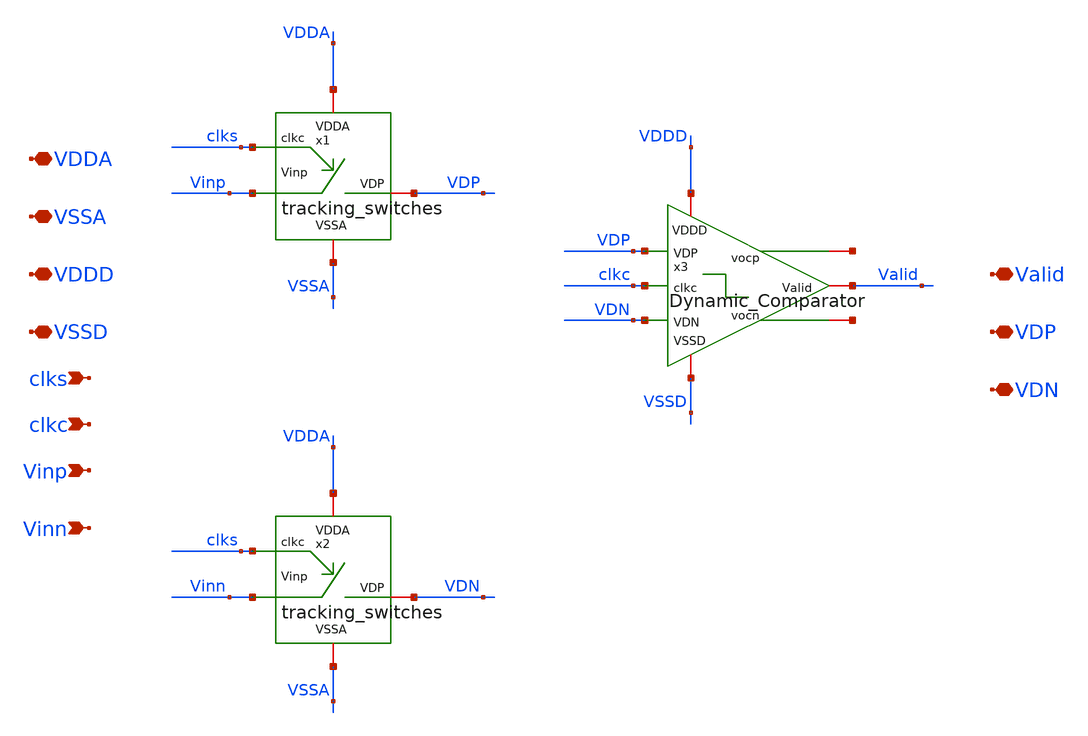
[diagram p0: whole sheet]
** sch_path: SAR_ADC/integration/TrackingSW_DynComp.sch
**.subckt TrackingSW_DynComp VDDD VSSD clks VDDA VSSA clkc Vinp Vinn Valid VDP VDN
*.iopin VDDD
*.iopin VSSD
*.ipin clks
*.iopin VDDA
*.iopin VSSA
*.ipin clkc
*.ipin Vinp
*.ipin Vinn
*.iopin Valid
*.iopin VDP
*.iopin VDN
x1 VDP VDDA VSSA clks Vinp tracking_switches
x2 VDN VDDA VSSA clks Vinn tracking_switches
x3 net1 net2 VDDD VSSD VDP VDN Valid clkc Dynamic_Comparator
**.ends
.end
